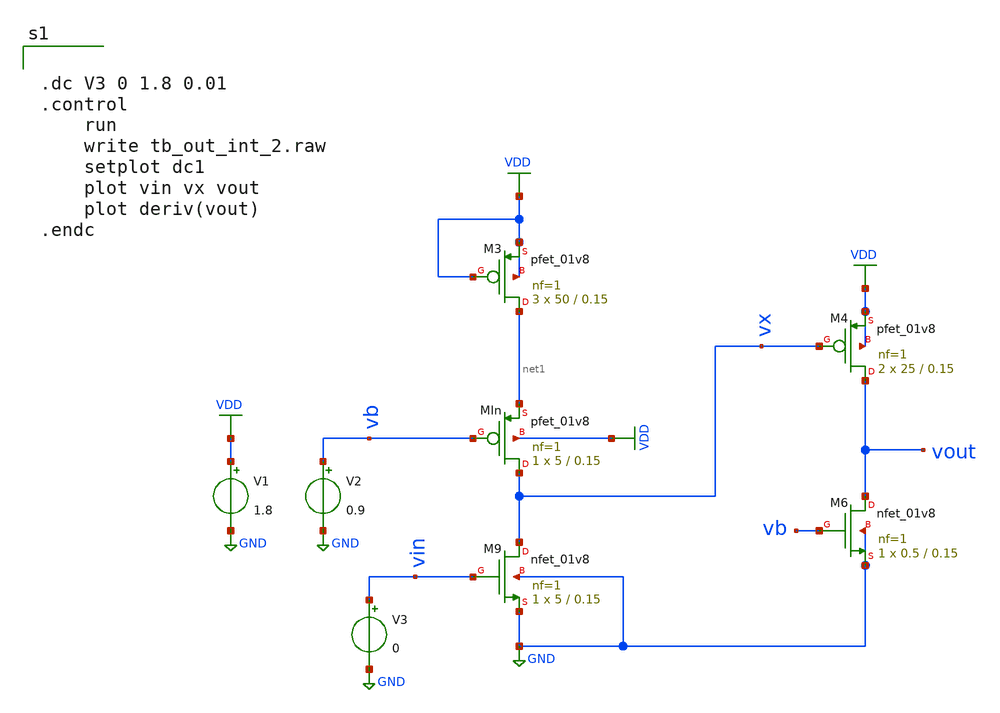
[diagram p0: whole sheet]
** sch_path: tb_out_int_2.sch
**.subckt tb_out_int_2
XMIn vx vb net1 VDD sky130_fd_pr__pfet_01v8 L=0.15 W=5 nf=1 ad='int((nf+1)/2) * W/nf * 0.29' as='int((nf+2)/2) * W/nf * 0.29'
+ pd='2*int((nf+1)/2) * (W/nf + 0.29)' ps='2*int((nf+2)/2) * (W/nf + 0.29)' nrd='0.29 / W' nrs='0.29 / W'
+ sa=0 sb=0 sd=0 mult=1 m=1
XM3 net1 VDD VDD VDD sky130_fd_pr__pfet_01v8 L=0.15 W=50 nf=1 ad='int((nf+1)/2) * W/nf * 0.29' as='int((nf+2)/2) * W/nf * 0.29'
+ pd='2*int((nf+1)/2) * (W/nf + 0.29)' ps='2*int((nf+2)/2) * (W/nf + 0.29)' nrd='0.29 / W' nrs='0.29 / W'
+ sa=0 sb=0 sd=0 mult=3 m=3
XM9 vx vin GND GND sky130_fd_pr__nfet_01v8 L=0.15 W=5 nf=1 ad='int((nf+1)/2) * W/nf * 0.29' as='int((nf+2)/2) * W/nf * 0.29'
+ pd='2*int((nf+1)/2) * (W/nf + 0.29)' ps='2*int((nf+2)/2) * (W/nf + 0.29)' nrd='0.29 / W' nrs='0.29 / W'
+ sa=0 sb=0 sd=0 mult=1 m=1
V1 VDD GND 1.8
V2 vb GND 0.9
V3 vin GND 0
XM4 vout vx VDD VDD sky130_fd_pr__pfet_01v8 L=0.15 W=25 nf=1 ad='int((nf+1)/2) * W/nf * 0.29' as='int((nf+2)/2) * W/nf * 0.29'
+ pd='2*int((nf+1)/2) * (W/nf + 0.29)' ps='2*int((nf+2)/2) * (W/nf + 0.29)' nrd='0.29 / W' nrs='0.29 / W'
+ sa=0 sb=0 sd=0 mult=2 m=2
XM6 vout vb GND GND sky130_fd_pr__nfet_01v8 L=0.15 W=0.5 nf=1 ad='int((nf+1)/2) * W/nf * 0.29' as='int((nf+2)/2) * W/nf * 0.29'
+ pd='2*int((nf+1)/2) * (W/nf + 0.29)' ps='2*int((nf+2)/2) * (W/nf + 0.29)' nrd='0.29 / W' nrs='0.29 / W'
+ sa=0 sb=0 sd=0 mult=1 m=1
**** begin user architecture code


.param mc_mm_switch=0
.param mc_pr_switch=0
.include /foss/pdks/sky130A/libs.tech/ngspice/corners/tt.spice
.include /foss/pdks/sky130A/libs.tech/ngspice/r+c/res_typical__cap_typical.spice
.include /foss/pdks/sky130A/libs.tech/ngspice/r+c/res_typical__cap_typical__lin.spice




.dc V3 0 1.8 0.01
.control
	run
	write tb_out_int_2.raw
	setplot dc1
	plot vin vx vout
	plot deriv(vout)
.endc



**** end user architecture code
**.ends
.GLOBAL GND
.GLOBAL VDD
.end
